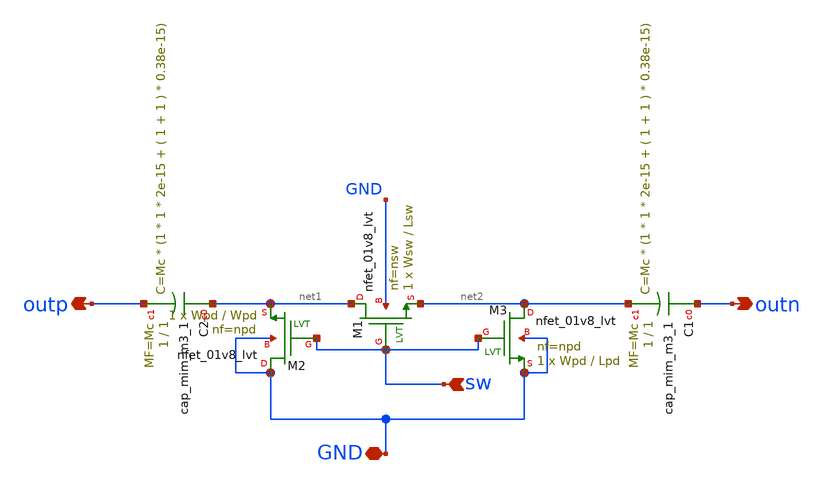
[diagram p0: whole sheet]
** sch_path: openfasoc/generators/lc-dco/xschem_rundir/swcap.sch
**.subckt swcap outn outp sw GND
*.opin outn
*.opin outp
*.ipin sw
*.iopin GND
XM1 net1 sw net2 GND sky130_fd_pr__nfet_01v8_lvt L=Lsw W=Wsw nf=nsw ad='int((nf+1)/2) * W/nf * 0.29'
+ as='int((nf+2)/2) * W/nf * 0.29' pd='2*int((nf+1)/2) * (W/nf + 0.29)' ps='2*int((nf+2)/2) * (W/nf + 0.29)'
+ nrd='0.29 / W' nrs='0.29 / W' sa=0 sb=0 sd=0 mult=1 m=1
XM2 GND sw net1 GND sky130_fd_pr__nfet_01v8_lvt L=Wpd W=Wpd nf=npd ad='int((nf+1)/2) * W/nf * 0.29' as='int((nf+2)/2) * W/nf * 0.29'
+ pd='2*int((nf+1)/2) * (W/nf + 0.29)' ps='2*int((nf+2)/2) * (W/nf + 0.29)' nrd='0.29 / W' nrs='0.29 / W'
+ sa=0 sb=0 sd=0 mult=1 m=1
XM3 net2 sw GND GND sky130_fd_pr__nfet_01v8_lvt L=Lpd W=Wpd nf=npd ad='int((nf+1)/2) * W/nf * 0.29' as='int((nf+2)/2) * W/nf * 0.29'
+ pd='2*int((nf+1)/2) * (W/nf + 0.29)' ps='2*int((nf+2)/2) * (W/nf + 0.29)' nrd='0.29 / W' nrs='0.29 / W'
+ sa=0 sb=0 sd=0 mult=1 m=1
XC1 outn net2 sky130_fd_pr__cap_mim_m3_1 W=1 L=1 MF=Mc m=Mc
XC2 net1 outp sky130_fd_pr__cap_mim_m3_1 W=1 L=1 MF=Mc m=Mc
**.ends
.end
